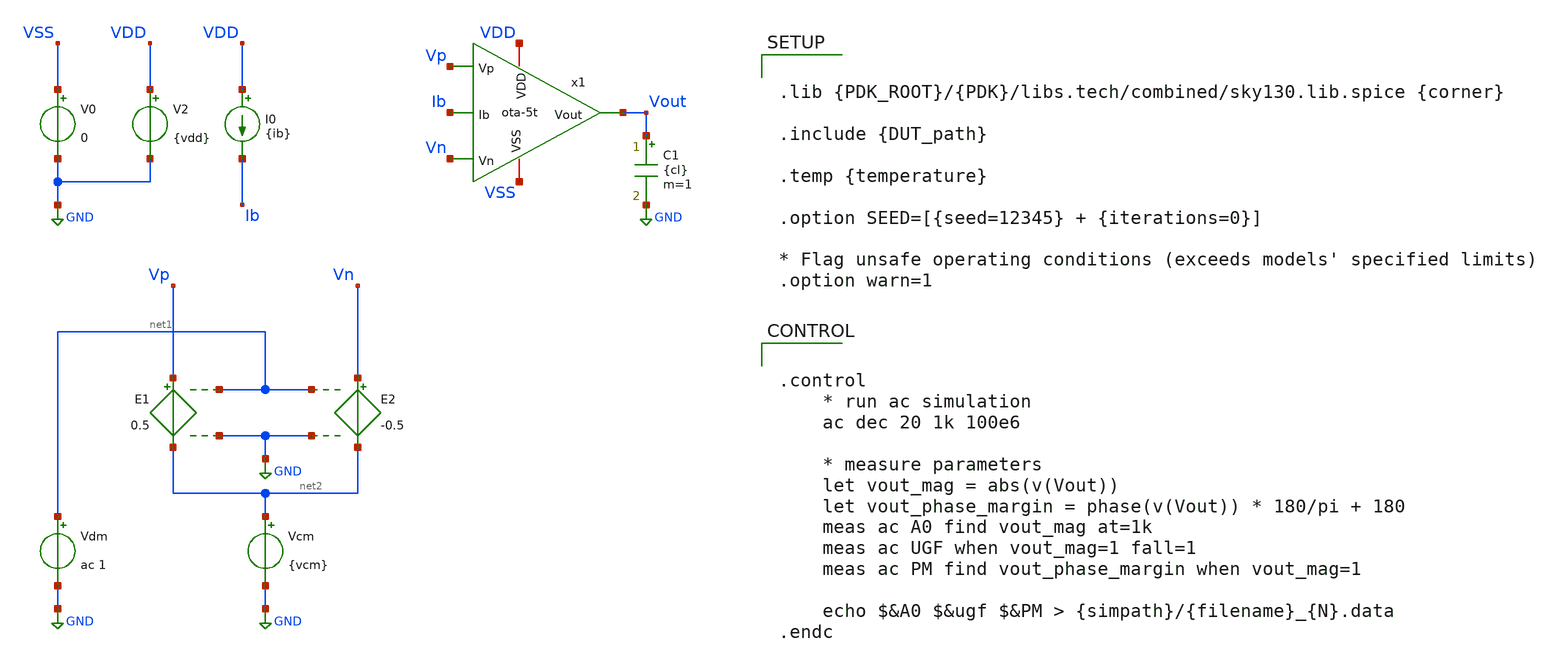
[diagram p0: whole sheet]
** sch_path: cace/templates/ac.sch
**.subckt ac
I0 VDD Ib {ib}
C1 Vout GND {cl} m=1
V0 VSS GND 0
V2 VDD GND {vdd}
E1 Vp net2 net1 GND 0.5
E2 Vn net2 net1 GND -0.5
Vdm net1 GND ac 1
Vcm net2 GND {vcm}
x1 Vp Vn Vout VDD VSS Ib ota-5t
**** begin user architecture code


.lib {PDK_ROOT}/{PDK}/libs.tech/combined/sky130.lib.spice {corner}

.include {DUT_path}

.temp {temperature}

.option SEED=[{seed=12345} + {iterations=0}]

* Flag unsafe operating conditions (exceeds models' specified limits)
.option warn=1




.control
    * run ac simulation
    ac dec 20 1k 100e6

    * measure parameters
    let vout_mag = abs(v(Vout))
    let vout_phase_margin = phase(v(Vout)) * 180/pi + 180
    meas ac A0 find vout_mag at=1k
    meas ac UGF when vout_mag=1 fall=1
    meas ac PM find vout_phase_margin when vout_mag=1

    echo $&A0 $&ugf $&PM > {simpath}/{filename}_{N}.data
.endc


**** end user architecture code
**.ends
.GLOBAL GND
.end
